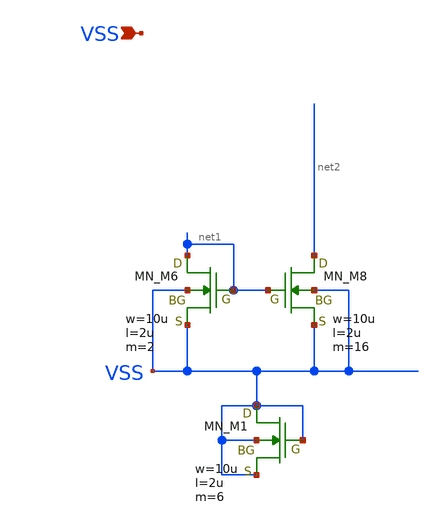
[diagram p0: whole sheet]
** sch_path: member_project/JJY_Receiver/Masahiro/jjy_recv/OBUF_SSF/NMOSCM.sch
**.subckt NMOSCM VSS
*.ipin VSS
XM6 net1 net1 VSS VSS NMOS w=10u l=2u as=0 ad=0 ps=0 pd=0 nrd=0 nrs=0 m=2
XM8 net2 net1 VSS VSS NMOS w=10u l=2u as=0 ad=0 ps=0 pd=0 nrd=0 nrs=0 m=16
XM1 VSS VSS VSS VSS NMOS w=10u l=2u as=0 ad=0 ps=0 pd=0 nrd=0 nrs=0 m=6
**.ends
.end
